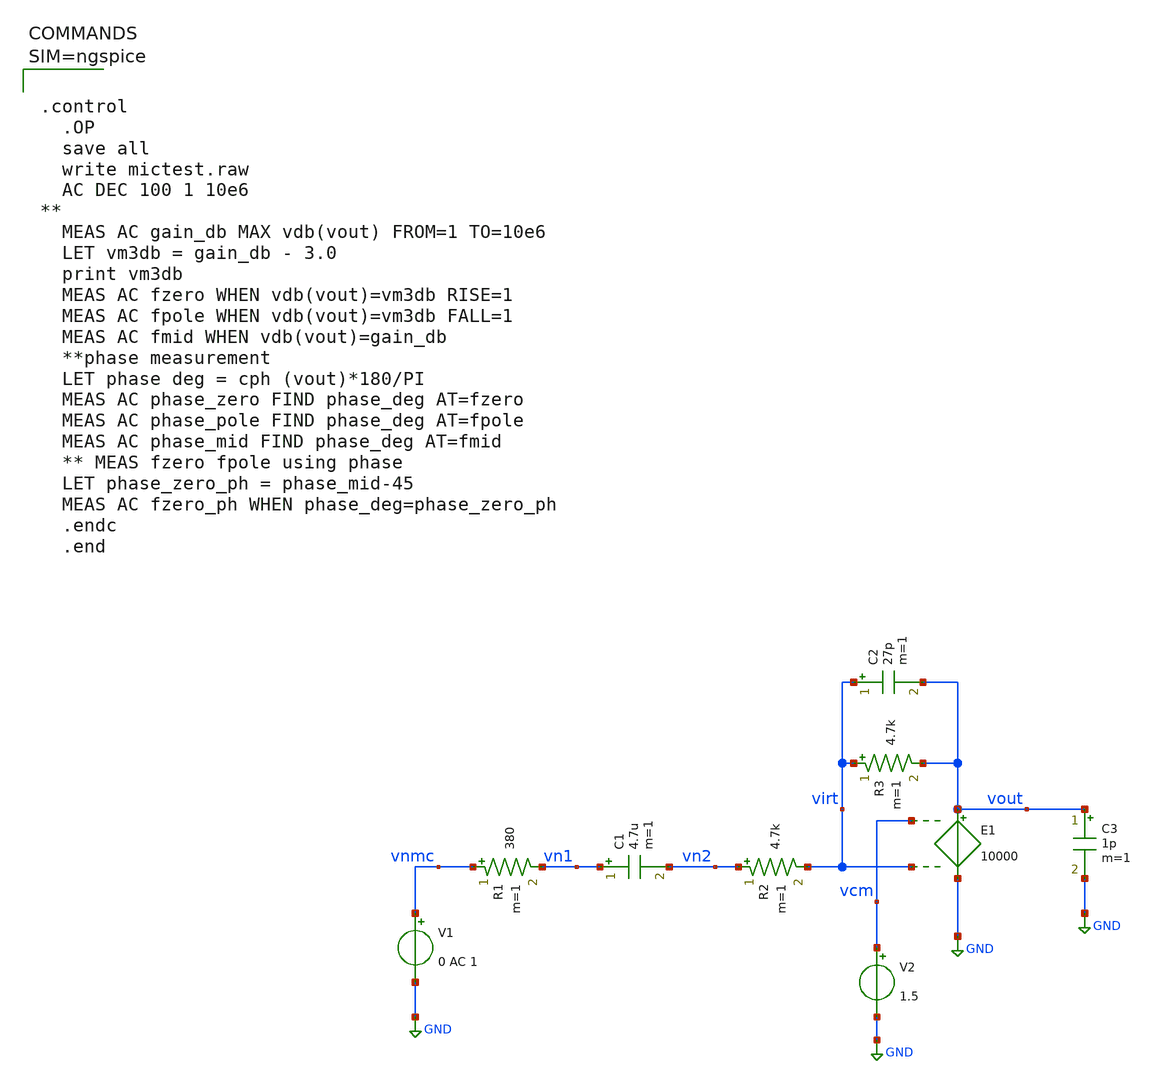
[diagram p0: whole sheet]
** sch_path: xschem/mictest.sch
**.subckt mictest
V1 vnmc GND 0 AC 1
C1 vn1 vn2 4.7u m=1
R1 vnmc vn1 380 m=1
R2 vn2 virt 4.7k m=1
E1 vout GND vcm virt 10000
R3 virt vout 4.7k m=1
C2 virt vout 27p m=1
V2 vcm GND 1.5
C3 vout GND 1p m=1
**** begin user architecture code



.control
  .OP
  save all
  write mictest.raw
  AC DEC 100 1 10e6
**
  MEAS AC gain_db MAX vdb(vout) FROM=1 TO=10e6
  LET vm3db = gain_db - 3.0
  print vm3db
  MEAS AC fzero WHEN vdb(vout)=vm3db RISE=1
  MEAS AC fpole WHEN vdb(vout)=vm3db FALL=1
  MEAS AC fmid WHEN vdb(vout)=gain_db
  **phase measurement
  LET phase deg = cph (vout)*180/PI
  MEAS AC phase_zero FIND phase_deg AT=fzero
  MEAS AC phase_pole FIND phase_deg AT=fpole
  MEAS AC phase_mid FIND phase_deg AT=fmid
  ** MEAS fzero fpole using phase
  LET phase_zero_ph = phase_mid-45
  MEAS AC fzero_ph WHEN phase_deg=phase_zero_ph
  .endc
  .end




**** end user architecture code
**.ends
.GLOBAL GND
.end
